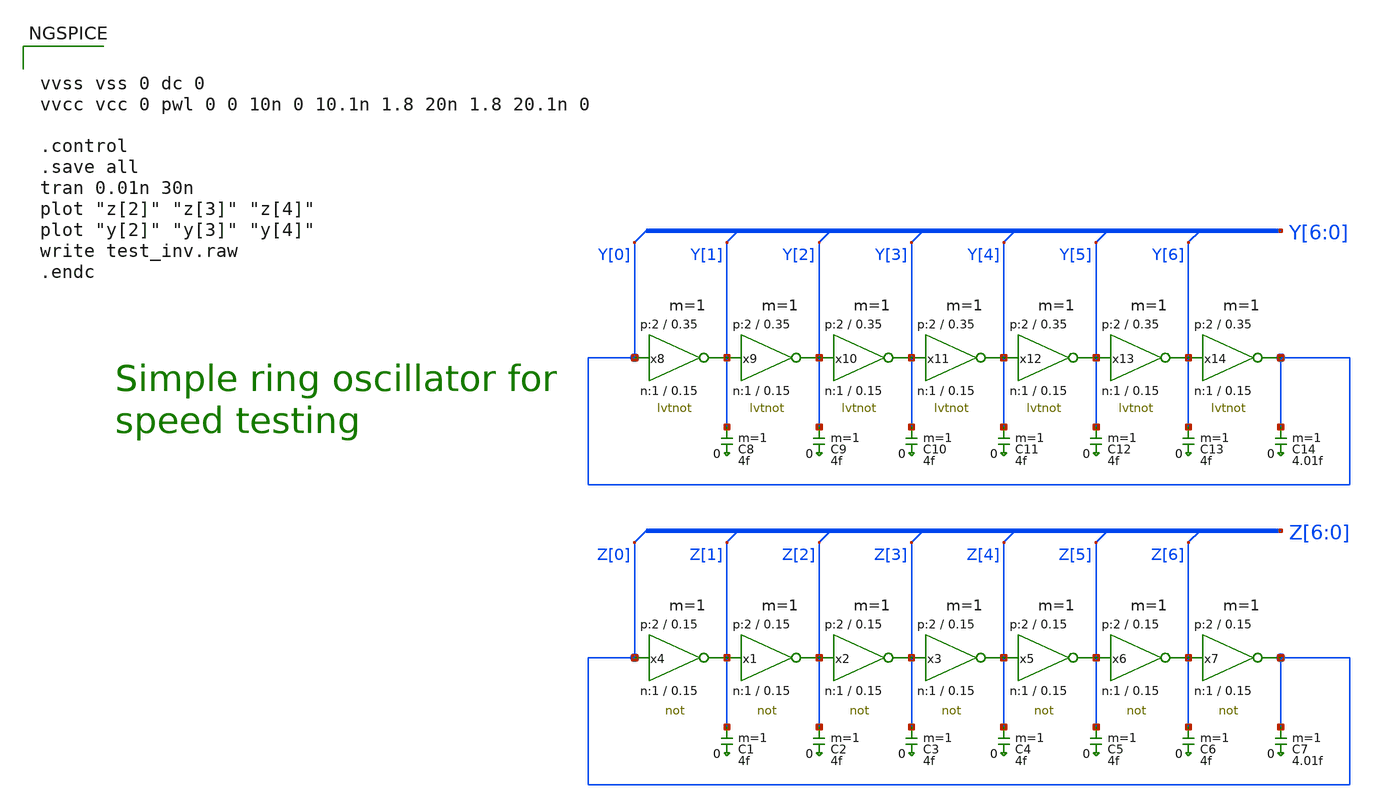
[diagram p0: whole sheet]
** sch_path: xyce/sky130A-xyce/libs.tech/xschem/sky130_tests/test_inv.sch
* Copyright 2020 Stefan Frederik Schippers
* Licensed under the Apache License, Version 2.0 (the "License");
* you may not use this file except in compliance with the License.
* You may obtain a copy of the License at
* https://www.apache.org/licenses/LICENSE-2.0
* Unless required by applicable law or agreed to in writing, software
* distributed under the License is distributed on an "AS IS" BASIS,
* WITHOUT WARRANTIES OR CONDITIONS OF ANY KIND, either express or implied.
* See the License for the specific language governing permissions and
* limitations under the License.
**.subckt test_inv
C1 Z[1] 0 4f m=1
C2 Z[2] 0 4f m=1
C3 Z[3] 0 4f m=1
C4 Z[4] 0 4f m=1
C5 Z[5] 0 4f m=1
C6 Z[6] 0 4f m=1
C7 Z[0] 0 4.01f m=1
C8 Y[1] 0 4f m=1
C9 Y[2] 0 4f m=1
C10 Y[3] 0 4f m=1
C11 Y[4] 0 4f m=1
C12 Y[5] 0 4f m=1
C13 Y[6] 0 4f m=1
C14 Y[0] 0 4.01f m=1
x4 Z[1] Z[0] VCC VSS not W_N=1 L_N=0.15 W_P=2 L_P=0.15 m=1
x1 Z[2] Z[1] VCC VSS not W_N=1 L_N=0.15 W_P=2 L_P=0.15 m=1
x2 Z[3] Z[2] VCC VSS not W_N=1 L_N=0.15 W_P=2 L_P=0.15 m=1
x3 Z[4] Z[3] VCC VSS not W_N=1 L_N=0.15 W_P=2 L_P=0.15 m=1
x5 Z[5] Z[4] VCC VSS not W_N=1 L_N=0.15 W_P=2 L_P=0.15 m=1
x6 Z[6] Z[5] VCC VSS not W_N=1 L_N=0.15 W_P=2 L_P=0.15 m=1
x7 Z[0] Z[6] VCC VSS not W_N=1 L_N=0.15 W_P=2 L_P=0.15 m=1
x8 Y[0] Y[1] VCC VSS lvtnot W_N=1 L_N=0.15 W_P=2 L_P=0.35 m=1
x9 Y[1] Y[2] VCC VSS lvtnot W_N=1 L_N=0.15 W_P=2 L_P=0.35 m=1
x10 Y[2] Y[3] VCC VSS lvtnot W_N=1 L_N=0.15 W_P=2 L_P=0.35 m=1
x11 Y[3] Y[4] VCC VSS lvtnot W_N=1 L_N=0.15 W_P=2 L_P=0.35 m=1
x12 Y[4] Y[5] VCC VSS lvtnot W_N=1 L_N=0.15 W_P=2 L_P=0.35 m=1
x13 Y[5] Y[6] VCC VSS lvtnot W_N=1 L_N=0.15 W_P=2 L_P=0.35 m=1
x14 Y[6] Y[0] VCC VSS lvtnot W_N=1 L_N=0.15 W_P=2 L_P=0.35 m=1
**** begin user architecture code


vvss vss 0 dc 0
vvcc vcc 0 pwl 0 0 10n 0 10.1n 1.8 20n 1.8 20.1n 0

.control
.save all
tran 0.01n 30n
plot "z[2]" "z[3]" "z[4]"
plot "y[2]" "y[3]" "y[4]"
write test_inv.raw
.endc



.include $::SKYWATER_MODELS/cells/nfet_01v8/sky130_fd_pr__nfet_01v8__tt.corner.spice
.include $::SKYWATER_MODELS/cells/nfet_01v8_lvt/sky130_fd_pr__nfet_01v8_lvt__tt.corner.spice
.include $::SKYWATER_MODELS/cells/pfet_01v8/sky130_fd_pr__pfet_01v8__tt.corner.spice
.include $::SKYWATER_MODELS/cells/nfet_03v3_nvt/sky130_fd_pr__nfet_03v3_nvt__tt.corner.spice
.include $::SKYWATER_MODELS/cells/nfet_05v0_nvt/sky130_fd_pr__nfet_05v0_nvt__tt.corner.spice
.include $::SKYWATER_MODELS/cells/esd_nfet_01v8/sky130_fd_pr__esd_nfet_01v8__tt.corner.spice
.include $::SKYWATER_MODELS/cells/pfet_01v8_lvt/sky130_fd_pr__pfet_01v8_lvt__tt.corner.spice
.include $::SKYWATER_MODELS/cells/pfet_01v8_hvt/sky130_fd_pr__pfet_01v8_hvt__tt.corner.spice
.include $::SKYWATER_MODELS/cells/esd_pfet_g5v0d10v5/sky130_fd_pr__esd_pfet_g5v0d10v5__tt.corner.spice
.include $::SKYWATER_MODELS/cells/pfet_g5v0d10v5/sky130_fd_pr__pfet_g5v0d10v5__tt.corner.spice
.include $::SKYWATER_MODELS/cells/pfet_g5v0d16v0/sky130_fd_pr__pfet_g5v0d16v0__tt.corner.spice
.include $::SKYWATER_MODELS/cells/nfet_g5v0d10v5/sky130_fd_pr__nfet_g5v0d10v5__tt.corner.spice
.include $::SKYWATER_MODELS/cells/nfet_g5v0d16v0/sky130_fd_pr__nfet_g5v0d16v0__tt_discrete.corner.spice
.include $::SKYWATER_MODELS/cells/esd_nfet_g5v0d10v5/sky130_fd_pr__esd_nfet_g5v0d10v5__tt.corner.spice
.include $::SKYWATER_MODELS/models/corners/tt/nonfet.spice
* Mismatch parameters
.include $::SKYWATER_MODELS/cells/nfet_01v8/sky130_fd_pr__nfet_01v8__mismatch.corner.spice
.include $::SKYWATER_MODELS/cells/pfet_01v8/sky130_fd_pr__pfet_01v8__mismatch.corner.spice
.include $::SKYWATER_MODELS/cells/nfet_01v8_lvt/sky130_fd_pr__nfet_01v8_lvt__mismatch.corner.spice
.include $::SKYWATER_MODELS/cells/pfet_01v8_lvt/sky130_fd_pr__pfet_01v8_lvt__mismatch.corner.spice
.include $::SKYWATER_MODELS/cells/pfet_01v8_hvt/sky130_fd_pr__pfet_01v8_hvt__mismatch.corner.spice
.include $::SKYWATER_MODELS/cells/nfet_g5v0d10v5/sky130_fd_pr__nfet_g5v0d10v5__mismatch.corner.spice
.include $::SKYWATER_MODELS/cells/pfet_g5v0d10v5/sky130_fd_pr__pfet_g5v0d10v5__mismatch.corner.spice
.include $::SKYWATER_MODELS/cells/nfet_05v0_nvt/sky130_fd_pr__nfet_05v0_nvt__mismatch.corner.spice
.include $::SKYWATER_MODELS/cells/nfet_03v3_nvt/sky130_fd_pr__nfet_03v3_nvt__mismatch.corner.spice
* Resistor$::SKYWATER_MODELS/Capacitor
.include $::SKYWATER_MODELS/models/r+c/res_typical__cap_typical.spice
.include $::SKYWATER_MODELS/models/r+c/res_typical__cap_typical__lin.spice
* Special cells
.include $::SKYWATER_MODELS/models/corners/tt/specialized_cells.spice
* All models
.include $::SKYWATER_MODELS/models/all.spice
* Corner
.include $::SKYWATER_MODELS/models/corners/tt/rf.spice

**** end user architecture code
**.ends

* expanding   symbol:  sky130_tests/not.sym # of pins=2
** sym_path: xyce/sky130A-xyce/libs.tech/xschem/sky130_tests/not.sym
** sch_path: xyce/sky130A-xyce/libs.tech/xschem/sky130_tests/not.sch
.subckt not y a VCCPIN VSSPIN     W_N=1 L_N=0.15 W_P=2 L_P=0.15
*.opin y
*.ipin a
XM1 y a VSSPIN VSSPIN sky130_fd_pr__nfet_01v8 L=L_N W=W_N nf=1 ad='int((nf+1)/2) * W/nf * 0.29' as='int((nf+2)/2) * W/nf * 0.29'
+ pd='2*int((nf+1)/2) * (W/nf + 0.29)' ps='2*int((nf+2)/2) * (W/nf + 0.29)' nrd='0.29 / W' nrs='0.29 / W'
+ sa=0 sb=0 sd=0 mult=1 m=1
XM2 y a VCCPIN VCCPIN sky130_fd_pr__pfet_01v8 L=L_P W=W_P nf=1 ad='int((nf+1)/2) * W/nf * 0.29' as='int((nf+2)/2) * W/nf * 0.29'
+ pd='2*int((nf+1)/2) * (W/nf + 0.29)' ps='2*int((nf+2)/2) * (W/nf + 0.29)' nrd='0.29 / W' nrs='0.29 / W'
+ sa=0 sb=0 sd=0 mult=1 m=1
.ends


* expanding   symbol:  sky130_tests/lvtnot.sym # of pins=2
** sym_path: xyce/sky130A-xyce/libs.tech/xschem/sky130_tests/lvtnot.sym
** sch_path: xyce/sky130A-xyce/libs.tech/xschem/sky130_tests/lvtnot.sch
.subckt lvtnot a y VCCPIN VSSPIN     W_N=1 L_N=0.15 W_P=2 L_P=0.35
*.opin y
*.ipin a
XM2 y a VCCPIN VCCPIN sky130_fd_pr__pfet_01v8_lvt L=L_P W=W_P nf=1 ad='int((nf+1)/2) * W/nf * 0.29' as='int((nf+2)/2) * W/nf * 0.29'
+ pd='2*int((nf+1)/2) * (W/nf + 0.29)' ps='2*int((nf+2)/2) * (W/nf + 0.29)' nrd='0.29 / W' nrs='0.29 / W'
+ sa=0 sb=0 sd=0 mult=1 m=1
XM1 y a VSSPIN VSSPIN sky130_fd_pr__nfet_01v8_lvt L=L_N W=W_N nf=1 ad='int((nf+1)/2) * W/nf * 0.29' as='int((nf+2)/2) * W/nf * 0.29'
+ pd='2*int((nf+1)/2) * (W/nf + 0.29)' ps='2*int((nf+2)/2) * (W/nf + 0.29)' nrd='0.29 / W' nrs='0.29 / W'
+ sa=0 sb=0 sd=0 mult=1 m=1
.ends

.end
